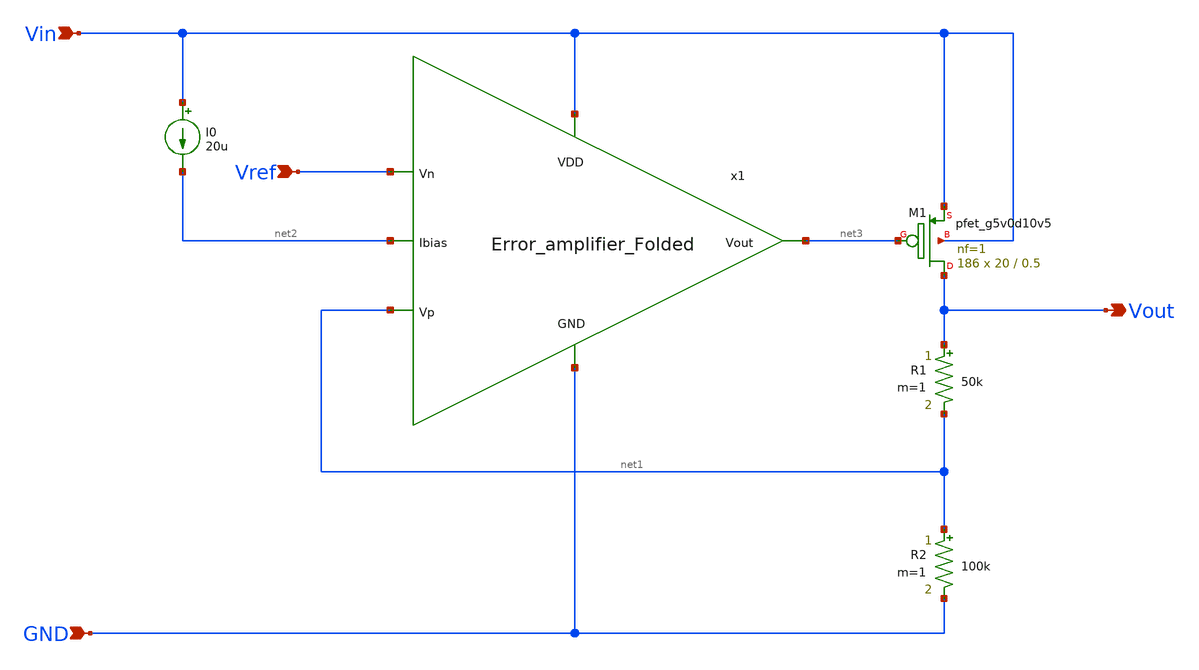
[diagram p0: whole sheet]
** sch_path: Analog_Blocks/LDO/Schematic/LDO_Miller_1.8v/LDO_test.sch
**.subckt LDO_test Vin GND Vout Vref
*.ipin Vin
*.ipin GND
*.opin Vout
*.ipin Vref
XM1 Vout net3 Vin Vin sky130_fd_pr__pfet_g5v0d10v5 L=0.5 W=20 nf=1 ad='int((nf+1)/2) * W/nf * 0.29' as='int((nf+2)/2) * W/nf * 0.29'
+ pd='2*int((nf+1)/2) * (W/nf + 0.29)' ps='2*int((nf+2)/2) * (W/nf + 0.29)' nrd='0.29 / W' nrs='0.29 / W'
+ sa=0 sb=0 sd=0 mult=186 m=186
R1 Vout net1 50k m=1
R2 net1 GND 100k m=1
I0 Vin net2 20u
x1 Vin net3 net1 Vref net2 GND Error_amplifier_Folded
**.ends

* expanding   symbol:
*+  /home/eslam/mabrains/Analog_blocks/Analog_Blocks/LDO/Schematic/LDO_Folded_1.8v/Error_amplifier_Folded.sym # of pins=6
** sym_path: Analog_Blocks/LDO/Schematic/LDO_Folded_1.8v/Error_amplifier_Folded.sym
** sch_path: Analog_Blocks/LDO/Schematic/LDO_Folded_1.8v/Error_amplifier_Folded.sch
.subckt Error_amplifier_Folded VDD Vout Vp Vn Ibias GND
*.ipin VDD
*.ipin GND
*.ipin Vp
*.ipin Vn
*.opin Vout
*.ipin Ibias
XM1 net3 Vp net1 GND sky130_fd_pr__nfet_g5v0d10v5 L=0.5 W=10 nf=1 ad='int((nf+1)/2) * W/nf * 0.29' as='int((nf+2)/2) * W/nf * 0.29'
+ pd='2*int((nf+1)/2) * (W/nf + 0.29)' ps='2*int((nf+2)/2) * (W/nf + 0.29)' nrd='0.29 / W' nrs='0.29 / W'
+ sa=0 sb=0 sd=0 mult=5 m=5
XM2 net2 Vn net1 GND sky130_fd_pr__nfet_g5v0d10v5 L=0.5 W=10 nf=1 ad='int((nf+1)/2) * W/nf * 0.29' as='int((nf+2)/2) * W/nf * 0.29'
+ pd='2*int((nf+1)/2) * (W/nf + 0.29)' ps='2*int((nf+2)/2) * (W/nf + 0.29)' nrd='0.29 / W' nrs='0.29 / W'
+ sa=0 sb=0 sd=0 mult=5 m=5
XM9 Vout net4 GND GND sky130_fd_pr__nfet_g5v0d10v5 L=1 W=3 nf=1 ad='int((nf+1)/2) * W/nf * 0.29' as='int((nf+2)/2) * W/nf * 0.29'
+ pd='2*int((nf+1)/2) * (W/nf + 0.29)' ps='2*int((nf+2)/2) * (W/nf + 0.29)' nrd='0.29 / W' nrs='0.29 / W'
+ sa=0 sb=0 sd=0 mult=2 m=2
XM4 net3 net5 VDD VDD sky130_fd_pr__pfet_g5v0d10v5 L=0.5 W=20 nf=1 ad='int((nf+1)/2) * W/nf * 0.29' as='int((nf+2)/2) * W/nf * 0.29'
+ pd='2*int((nf+1)/2) * (W/nf + 0.29)' ps='2*int((nf+2)/2) * (W/nf + 0.29)' nrd='0.29 / W' nrs='0.29 / W'
+ sa=0 sb=0 sd=0 mult=2 m=2
XM3 net1 Ibias GND GND sky130_fd_pr__nfet_g5v0d10v5 L=1 W=3 nf=1 ad='int((nf+1)/2) * W/nf * 0.29' as='int((nf+2)/2) * W/nf * 0.29'
+ pd='2*int((nf+1)/2) * (W/nf + 0.29)' ps='2*int((nf+2)/2) * (W/nf + 0.29)' nrd='0.29 / W' nrs='0.29 / W'
+ sa=0 sb=0 sd=0 mult=4 m=4
XM8 net4 net4 GND GND sky130_fd_pr__nfet_g5v0d10v5 L=1 W=3 nf=1 ad='int((nf+1)/2) * W/nf * 0.29' as='int((nf+2)/2) * W/nf * 0.29'
+ pd='2*int((nf+1)/2) * (W/nf + 0.29)' ps='2*int((nf+2)/2) * (W/nf + 0.29)' nrd='0.29 / W' nrs='0.29 / W'
+ sa=0 sb=0 sd=0 mult=2 m=2
XM10 Ibias Ibias GND GND sky130_fd_pr__nfet_g5v0d10v5 L=1 W=3 nf=1 ad='int((nf+1)/2) * W/nf * 0.29' as='int((nf+2)/2) * W/nf * 0.29'
+ pd='2*int((nf+1)/2) * (W/nf + 0.29)' ps='2*int((nf+2)/2) * (W/nf + 0.29)' nrd='0.29 / W' nrs='0.29 / W'
+ sa=0 sb=0 sd=0 mult=4 m=4
XM11 net5 Ibias GND GND sky130_fd_pr__nfet_g5v0d10v5 L=1 W=3 nf=1 ad='int((nf+1)/2) * W/nf * 0.29' as='int((nf+2)/2) * W/nf * 0.29'
+ pd='2*int((nf+1)/2) * (W/nf + 0.29)' ps='2*int((nf+2)/2) * (W/nf + 0.29)' nrd='0.29 / W' nrs='0.29 / W'
+ sa=0 sb=0 sd=0 mult=2 m=2
XM12 net6 Ibias GND GND sky130_fd_pr__nfet_g5v0d10v5 L=1 W=3 nf=1 ad='int((nf+1)/2) * W/nf * 0.29' as='int((nf+2)/2) * W/nf * 0.29'
+ pd='2*int((nf+1)/2) * (W/nf + 0.29)' ps='2*int((nf+2)/2) * (W/nf + 0.29)' nrd='0.29 / W' nrs='0.29 / W'
+ sa=0 sb=0 sd=0 mult=2 m=2
XM13 net5 net5 VDD VDD sky130_fd_pr__pfet_g5v0d10v5 L=0.5 W=7 nf=1 ad='int((nf+1)/2) * W/nf * 0.29' as='int((nf+2)/2) * W/nf * 0.29'
+ pd='2*int((nf+1)/2) * (W/nf + 0.29)' ps='2*int((nf+2)/2) * (W/nf + 0.29)' nrd='0.29 / W' nrs='0.29 / W'
+ sa=0 sb=0 sd=0 mult=2 m=2
XM14 net6 net6 VDD VDD sky130_fd_pr__pfet_g5v0d10v5 L=1 W=1 nf=1 ad='int((nf+1)/2) * W/nf * 0.29' as='int((nf+2)/2) * W/nf * 0.29'
+ pd='2*int((nf+1)/2) * (W/nf + 0.29)' ps='2*int((nf+2)/2) * (W/nf + 0.29)' nrd='0.29 / W' nrs='0.29 / W'
+ sa=0 sb=0 sd=0 mult=2 m=2
XM5 net2 net5 VDD VDD sky130_fd_pr__pfet_g5v0d10v5 L=0.5 W=20 nf=1 ad='int((nf+1)/2) * W/nf * 0.29' as='int((nf+2)/2) * W/nf * 0.29'
+ pd='2*int((nf+1)/2) * (W/nf + 0.29)' ps='2*int((nf+2)/2) * (W/nf + 0.29)' nrd='0.29 / W' nrs='0.29 / W'
+ sa=0 sb=0 sd=0 mult=2 m=2
XM6 net4 net6 net3 VDD sky130_fd_pr__pfet_g5v0d10v5 L=0.5 W=20 nf=1 ad='int((nf+1)/2) * W/nf * 0.29'
+ as='int((nf+2)/2) * W/nf * 0.29' pd='2*int((nf+1)/2) * (W/nf + 0.29)' ps='2*int((nf+2)/2) * (W/nf + 0.29)'
+ nrd='0.29 / W' nrs='0.29 / W' sa=0 sb=0 sd=0 mult=2 m=2
XM7 Vout net6 net2 VDD sky130_fd_pr__pfet_g5v0d10v5 L=0.5 W=20 nf=1 ad='int((nf+1)/2) * W/nf * 0.29'
+ as='int((nf+2)/2) * W/nf * 0.29' pd='2*int((nf+1)/2) * (W/nf + 0.29)' ps='2*int((nf+2)/2) * (W/nf + 0.29)'
+ nrd='0.29 / W' nrs='0.29 / W' sa=0 sb=0 sd=0 mult=2 m=2
.ends

.end
